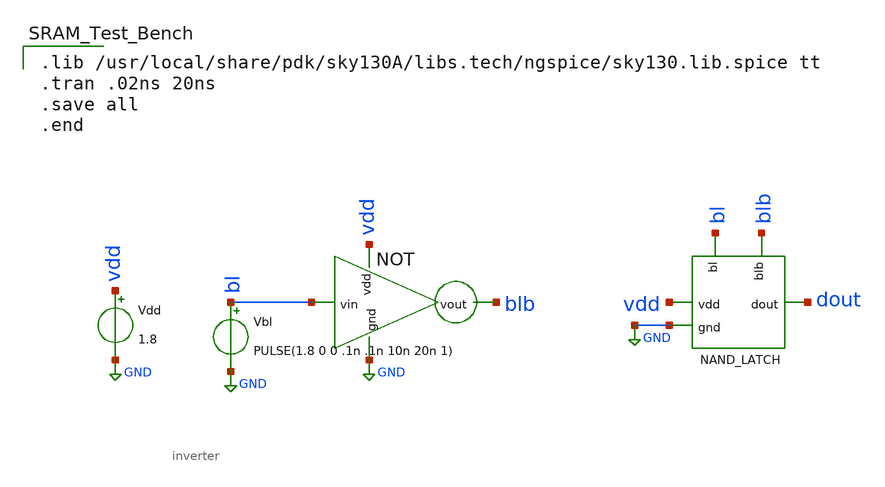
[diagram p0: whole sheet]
** sch_path: Projects/Schematic_Design_and_Analysis_of_an_8-Word_8-Bit_Static_RAM_with_6T_Storage_Cells_using_SKY130PDK/assets/schematic/nand_latch_tb.sch
**.subckt nand_latch_tb
x49 dout vdd GND bl blb nand_latch
Vdd vdd GND 1.8
Vbl bl GND PULSE(1.8 0 0 .1n .1n 10n 20n 1)
x20 vdd GND blb bl inverter
**** begin user architecture code

.lib /usr/local/share/pdk/sky130A/libs.tech/ngspice/sky130.lib.spice tt
.tran .02ns 20ns
.save all
.end

**** end user architecture code
**.ends

* expanding   symbol:  nand_latch.sym # of pins=5
** sym_path: Projects/Schematic_Design_and_Analysis_of_an_8-Word_8-Bit_Static_RAM_with_6T_Storage_Cells_using_SKY130PDK/assets/schematic/nand_latch.sym
** sch_path: Projects/Schematic_Design_and_Analysis_of_an_8-Word_8-Bit_Static_RAM_with_6T_Storage_Cells_using_SKY130PDK/assets/schematic/nand_latch.sch
.subckt nand_latch dout vdd gnd bl blb
*.ipin vdd
*.opin dout
*.ipin bl
*.ipin blb
*.ipin gnd
XM1 net1 dout net2 gnd sky130_fd_pr__nfet_01v8 L=0.15 W=2 nf=1 ad='int((nf+1)/2) * W/nf * 0.29' as='int((nf+2)/2) * W/nf * 0.29'
+ pd='2*int((nf+1)/2) * (W/nf + 0.29)' ps='2*int((nf+2)/2) * (W/nf + 0.29)' nrd='0.29 / W' nrs='0.29 / W'
+ sa=0 sb=0 sd=0 mult=1 m=1
XM2 net1 dout vdd vdd sky130_fd_pr__pfet_01v8 L=0.15 W=2 nf=1 ad='int((nf+1)/2) * W/nf * 0.29' as='int((nf+2)/2) * W/nf * 0.29'
+ pd='2*int((nf+1)/2) * (W/nf + 0.29)' ps='2*int((nf+2)/2) * (W/nf + 0.29)' nrd='0.29 / W' nrs='0.29 / W'
+ sa=0 sb=0 sd=0 mult=1 m=1
XM3 net1 bl vdd vdd sky130_fd_pr__pfet_01v8 L=0.15 W=2 nf=1 ad='int((nf+1)/2) * W/nf * 0.29' as='int((nf+2)/2) * W/nf * 0.29'
+ pd='2*int((nf+1)/2) * (W/nf + 0.29)' ps='2*int((nf+2)/2) * (W/nf + 0.29)' nrd='0.29 / W' nrs='0.29 / W'
+ sa=0 sb=0 sd=0 mult=1 m=1
XM4 net2 bl gnd gnd sky130_fd_pr__nfet_01v8 L=0.15 W=2 nf=1 ad='int((nf+1)/2) * W/nf * 0.29' as='int((nf+2)/2) * W/nf * 0.29'
+ pd='2*int((nf+1)/2) * (W/nf + 0.29)' ps='2*int((nf+2)/2) * (W/nf + 0.29)' nrd='0.29 / W' nrs='0.29 / W'
+ sa=0 sb=0 sd=0 mult=1 m=1
XM5 dout net1 net3 gnd sky130_fd_pr__nfet_01v8 L=0.15 W=2 nf=1 ad='int((nf+1)/2) * W/nf * 0.29' as='int((nf+2)/2) * W/nf * 0.29'
+ pd='2*int((nf+1)/2) * (W/nf + 0.29)' ps='2*int((nf+2)/2) * (W/nf + 0.29)' nrd='0.29 / W' nrs='0.29 / W'
+ sa=0 sb=0 sd=0 mult=1 m=1
XM6 dout net1 vdd vdd sky130_fd_pr__pfet_01v8 L=0.15 W=2 nf=1 ad='int((nf+1)/2) * W/nf * 0.29' as='int((nf+2)/2) * W/nf * 0.29'
+ pd='2*int((nf+1)/2) * (W/nf + 0.29)' ps='2*int((nf+2)/2) * (W/nf + 0.29)' nrd='0.29 / W' nrs='0.29 / W'
+ sa=0 sb=0 sd=0 mult=1 m=1
XM7 dout blb vdd vdd sky130_fd_pr__pfet_01v8 L=0.15 W=2 nf=1 ad='int((nf+1)/2) * W/nf * 0.29' as='int((nf+2)/2) * W/nf * 0.29'
+ pd='2*int((nf+1)/2) * (W/nf + 0.29)' ps='2*int((nf+2)/2) * (W/nf + 0.29)' nrd='0.29 / W' nrs='0.29 / W'
+ sa=0 sb=0 sd=0 mult=1 m=1
XM8 net3 blb gnd gnd sky130_fd_pr__nfet_01v8 L=0.15 W=2 nf=1 ad='int((nf+1)/2) * W/nf * 0.29' as='int((nf+2)/2) * W/nf * 0.29'
+ pd='2*int((nf+1)/2) * (W/nf + 0.29)' ps='2*int((nf+2)/2) * (W/nf + 0.29)' nrd='0.29 / W' nrs='0.29 / W'
+ sa=0 sb=0 sd=0 mult=1 m=1
.ends


* expanding   symbol:  inverter.sym # of pins=4
** sym_path: Projects/Schematic_Design_and_Analysis_of_an_8-Word_8-Bit_Static_RAM_with_6T_Storage_Cells_using_SKY130PDK/assets/schematic/inverter.sym
** sch_path: Projects/Schematic_Design_and_Analysis_of_an_8-Word_8-Bit_Static_RAM_with_6T_Storage_Cells_using_SKY130PDK/assets/schematic/inverter.sch
.subckt inverter vdd gnd vout vin
*.ipin vin
*.ipin vdd
*.ipin gnd
*.opin vout
XM1 vout vin gnd gnd sky130_fd_pr__nfet_01v8 L=0.15 W=1 nf=1 ad='int((nf+1)/2) * W/nf * 0.29' as='int((nf+2)/2) * W/nf * 0.29'
+ pd='2*int((nf+1)/2) * (W/nf + 0.29)' ps='2*int((nf+2)/2) * (W/nf + 0.29)' nrd='0.29 / W' nrs='0.29 / W'
+ sa=0 sb=0 sd=0 mult=1 m=1
XM2 vout vin vdd vdd sky130_fd_pr__pfet_01v8 L=0.15 W=2 nf=1 ad='int((nf+1)/2) * W/nf * 0.29' as='int((nf+2)/2) * W/nf * 0.29'
+ pd='2*int((nf+1)/2) * (W/nf + 0.29)' ps='2*int((nf+2)/2) * (W/nf + 0.29)' nrd='0.29 / W' nrs='0.29 / W'
+ sa=0 sb=0 sd=0 mult=1 m=1
.ends

.GLOBAL GND
.end
